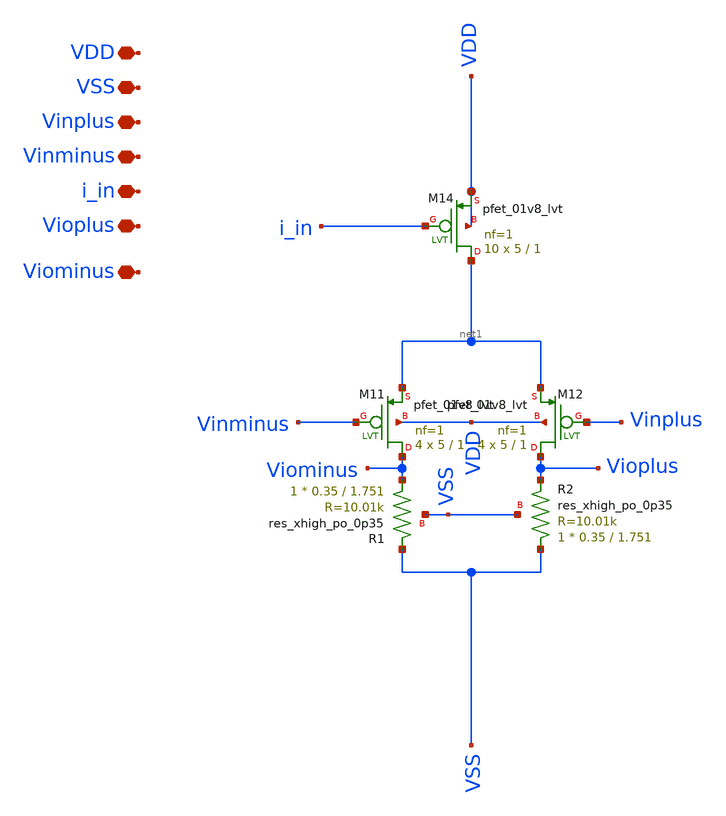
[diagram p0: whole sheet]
** sch_path: xschem/Preamp_noBias.sch
**.subckt Preamp_noBias VDD VSS Vinplus Vinminus Vioplus Viominus i_in
*.iopin VDD
*.iopin VSS
*.iopin Vinplus
*.iopin Vinminus
*.iopin Vioplus
*.iopin Viominus
*.iopin i_in
XM11 Viominus Vinminus net1 VDD sky130_fd_pr__pfet_01v8_lvt L=1 W=5 nf=1 ad='int((nf+1)/2) * W/nf * 0.29'
+ as='int((nf+2)/2) * W/nf * 0.29' pd='2*int((nf+1)/2) * (W/nf + 0.29)' ps='2*int((nf+2)/2) * (W/nf + 0.29)'
+ nrd='0.29 / W' nrs='0.29 / W' sa=0 sb=0 sd=0 mult=4 m=4
XM12 Vioplus Vinplus net1 VDD sky130_fd_pr__pfet_01v8_lvt L=1 W=5 nf=1 ad='int((nf+1)/2) * W/nf * 0.29'
+ as='int((nf+2)/2) * W/nf * 0.29' pd='2*int((nf+1)/2) * (W/nf + 0.29)' ps='2*int((nf+2)/2) * (W/nf + 0.29)'
+ nrd='0.29 / W' nrs='0.29 / W' sa=0 sb=0 sd=0 mult=4 m=4
XM14 net1 i_in VDD VDD sky130_fd_pr__pfet_01v8_lvt L=1 W=5 nf=1 ad='int((nf+1)/2) * W/nf * 0.29' as='int((nf+2)/2) * W/nf * 0.29'
+ pd='2*int((nf+1)/2) * (W/nf + 0.29)' ps='2*int((nf+2)/2) * (W/nf + 0.29)' nrd='0.29 / W' nrs='0.29 / W'
+ sa=0 sb=0 sd=0 mult=10 m=10
XR2 VSS Vioplus VSS sky130_fd_pr__res_xhigh_po_0p35 L=1.751 mult=1 m=1
XR1 Viominus VSS VSS sky130_fd_pr__res_xhigh_po_0p35 L=1.751 mult=1 m=1
**.ends
.end
